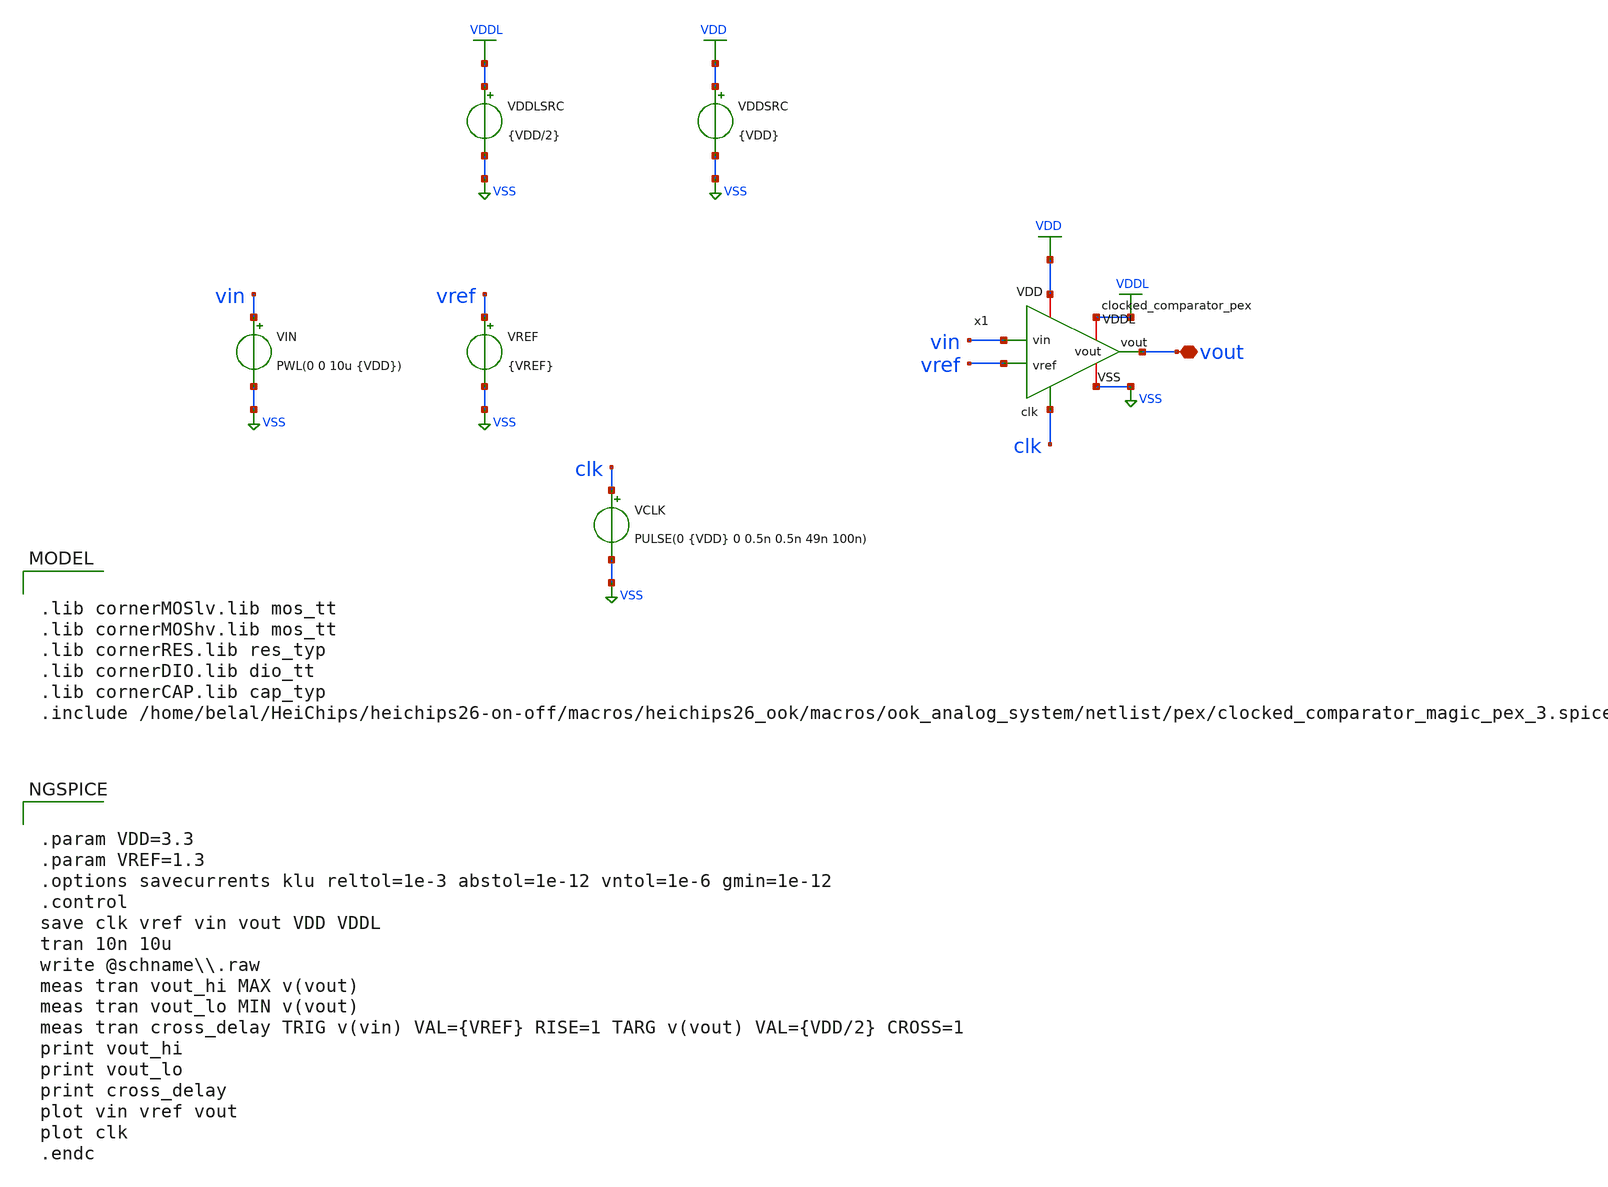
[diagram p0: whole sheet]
** sch_path: macros/heichips26_ook/macros/ook_analog_system/testbenches/xschem/clocked_comparator_tb_tran.sch
**.subckt clocked_comparator_tb_tran vout
*.iopin vout
x1 clk vref VDDL VDD vin vout VSS clocked_comparator_pex
VCLK clk VSS PULSE(0 {VDD} 0 0.5n 0.5n 49n 100n)
VDDSRC VDD VSS {VDD}
VDDLSRC VDDL VSS {VDD/2}
VREF vref VSS {VREF}
VIN vin VSS PWL(0 0 10u {VDD})
**** begin user architecture code


.param VDD=3.3
.param VREF=1.3
.options savecurrents klu reltol=1e-3 abstol=1e-12 vntol=1e-6 gmin=1e-12
.control
save clk vref vin vout VDD VDDL
tran 10n 10u
write @schname\\.raw
meas tran vout_hi MAX v(vout)
meas tran vout_lo MIN v(vout)
meas tran cross_delay TRIG v(vin) VAL={VREF} RISE=1 TARG v(vout) VAL={VDD/2} CROSS=1
print vout_hi
print vout_lo
print cross_delay
plot vin vref vout
plot clk
.endc


.lib cornerMOSlv.lib mos_tt
.lib cornerMOShv.lib mos_tt
.lib cornerRES.lib res_typ
.lib cornerDIO.lib dio_tt
.lib cornerCAP.lib cap_typ
.include /home/belal/HeiChips/heichips26-on-off/macros/heichips26_ook/macros/ook_analog_system/netlist/pex/clocked_comparator_magic_pex_3.spice

**** end user architecture code
**.ends
.GLOBAL VDD
.GLOBAL VDDL
.GLOBAL VSS
.end
